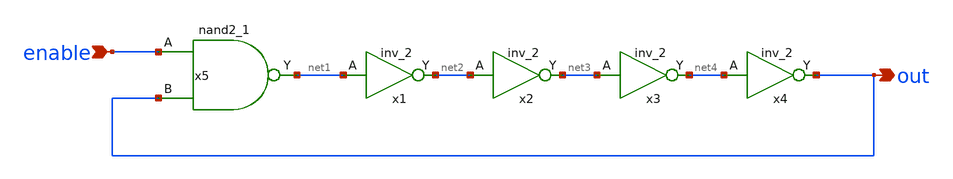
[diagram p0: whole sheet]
** sch_path: hgu/tutorial/ringoscill.sch
**.subckt ringoscill enable out
*.ipin enable
*.opin out
x1 net1 VGND VNB VPB VPWR net2 sky130_fd_sc_hd__inv_2
x2 net2 VGND VNB VPB VPWR net3 sky130_fd_sc_hd__inv_2
x3 net3 VGND VNB VPB VPWR net4 sky130_fd_sc_hd__inv_2
x4 net4 VGND VNB VPB VPWR out sky130_fd_sc_hd__inv_2
x5 enable out VGND VNB VPB VPWR net1 sky130_fd_sc_hd__nand2_1
**.ends
.end
